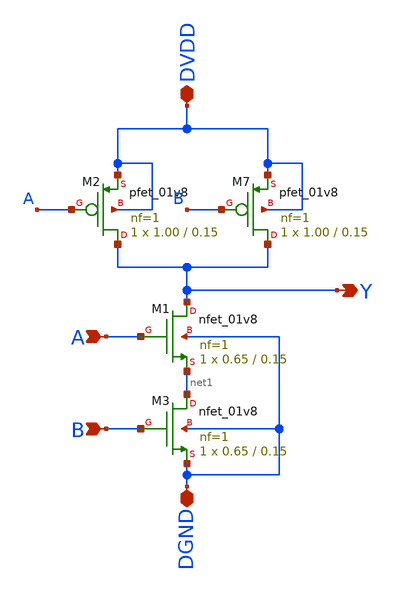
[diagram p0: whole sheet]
** sch_path: project/sch_sym_files/nand2.sch
**.subckt nand2 Y A DVDD DGND B
*.opin Y
*.ipin A
*.iopin DVDD
*.iopin DGND
*.ipin B
XM2 Y A DVDD DVDD sky130_fd_pr__pfet_01v8 L=0.15 W=1.00 nf=1 ad='int((nf+1)/2) * W/nf * 0.29' as='int((nf+2)/2) * W/nf * 0.29'
+ pd='2*int((nf+1)/2) * (W/nf + 0.29)' ps='2*int((nf+2)/2) * (W/nf + 0.29)' nrd='0.29 / W' nrs='0.29 / W'
+ sa=0 sb=0 sd=0 mult=1 m=1
XM1 Y A net1 DGND sky130_fd_pr__nfet_01v8 L=0.15 W=0.65 nf=1 ad='int((nf+1)/2) * W/nf * 0.29' as='int((nf+2)/2) * W/nf * 0.29'
+ pd='2*int((nf+1)/2) * (W/nf + 0.29)' ps='2*int((nf+2)/2) * (W/nf + 0.29)' nrd='0.29 / W' nrs='0.29 / W'
+ sa=0 sb=0 sd=0 mult=1 m=1
XM3 net1 B DGND DGND sky130_fd_pr__nfet_01v8 L=0.15 W=0.65 nf=1 ad='int((nf+1)/2) * W/nf * 0.29' as='int((nf+2)/2) * W/nf * 0.29'
+ pd='2*int((nf+1)/2) * (W/nf + 0.29)' ps='2*int((nf+2)/2) * (W/nf + 0.29)' nrd='0.29 / W' nrs='0.29 / W'
+ sa=0 sb=0 sd=0 mult=1 m=1
XM7 Y B DVDD DVDD sky130_fd_pr__pfet_01v8 L=0.15 W=1.00 nf=1 ad='int((nf+1)/2) * W/nf * 0.29' as='int((nf+2)/2) * W/nf * 0.29'
+ pd='2*int((nf+1)/2) * (W/nf + 0.29)' ps='2*int((nf+2)/2) * (W/nf + 0.29)' nrd='0.29 / W' nrs='0.29 / W'
+ sa=0 sb=0 sd=0 mult=1 m=1
**.ends
.end
